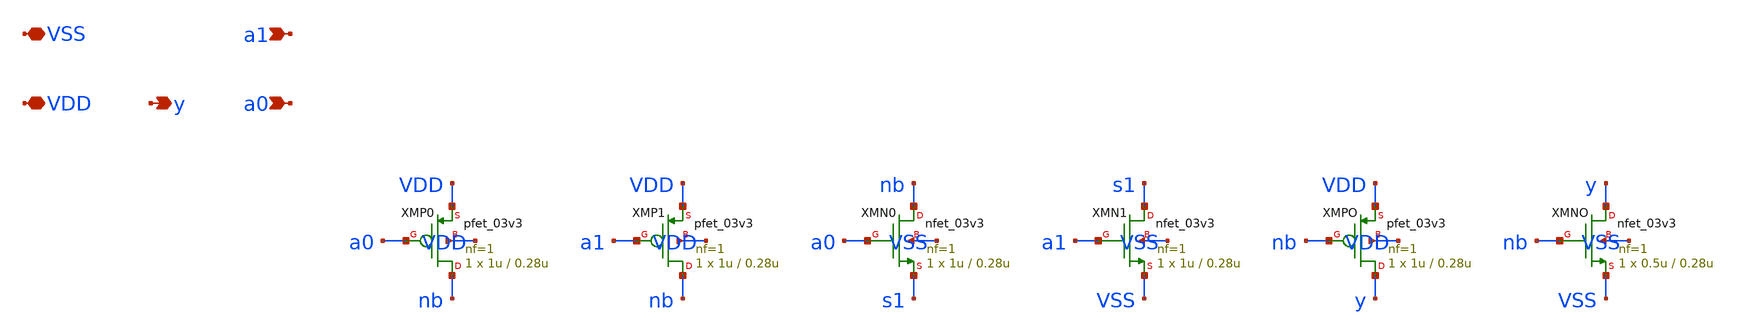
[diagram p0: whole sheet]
** sch_path: design/and2.sch
**.subckt and2 a0 a1 y VDD VSS
*.ipin a0
*.ipin a1
*.opin y
*.iopin VDD
*.iopin VSS
XMP0 nb a0 VDD VDD pfet_03v3 L=0.28u W=1u nf=1 ad='int((nf+1)/2) * W/nf * 0.18u' as='int((nf+2)/2) * W/nf * 0.18u'
+ pd='2*int((nf+1)/2) * (W/nf + 0.18u)' ps='2*int((nf+2)/2) * (W/nf + 0.18u)' nrd='0.18u / W' nrs='0.18u / W'
+ sa=0 sb=0 sd=0 m=1
XMP1 nb a1 VDD VDD pfet_03v3 L=0.28u W=1u nf=1 ad='int((nf+1)/2) * W/nf * 0.18u' as='int((nf+2)/2) * W/nf * 0.18u'
+ pd='2*int((nf+1)/2) * (W/nf + 0.18u)' ps='2*int((nf+2)/2) * (W/nf + 0.18u)' nrd='0.18u / W' nrs='0.18u / W'
+ sa=0 sb=0 sd=0 m=1
XMN0 nb a0 s1 VSS nfet_03v3 L=0.28u W=1u nf=1 ad='int((nf+1)/2) * W/nf * 0.18u' as='int((nf+2)/2) * W/nf * 0.18u'
+ pd='2*int((nf+1)/2) * (W/nf + 0.18u)' ps='2*int((nf+2)/2) * (W/nf + 0.18u)' nrd='0.18u / W' nrs='0.18u / W'
+ sa=0 sb=0 sd=0 m=1
XMN1 s1 a1 VSS VSS nfet_03v3 L=0.28u W=1u nf=1 ad='int((nf+1)/2) * W/nf * 0.18u' as='int((nf+2)/2) * W/nf * 0.18u'
+ pd='2*int((nf+1)/2) * (W/nf + 0.18u)' ps='2*int((nf+2)/2) * (W/nf + 0.18u)' nrd='0.18u / W' nrs='0.18u / W'
+ sa=0 sb=0 sd=0 m=1
XMPO y nb VDD VDD pfet_03v3 L=0.28u W=1u nf=1 ad='int((nf+1)/2) * W/nf * 0.18u' as='int((nf+2)/2) * W/nf * 0.18u'
+ pd='2*int((nf+1)/2) * (W/nf + 0.18u)' ps='2*int((nf+2)/2) * (W/nf + 0.18u)' nrd='0.18u / W' nrs='0.18u / W'
+ sa=0 sb=0 sd=0 m=1
XMNO y nb VSS VSS nfet_03v3 L=0.28u W=0.5u nf=1 ad='int((nf+1)/2) * W/nf * 0.18u' as='int((nf+2)/2) * W/nf * 0.18u'
+ pd='2*int((nf+1)/2) * (W/nf + 0.18u)' ps='2*int((nf+2)/2) * (W/nf + 0.18u)' nrd='0.18u / W' nrs='0.18u / W'
+ sa=0 sb=0 sd=0 m=1
**.ends
.end
